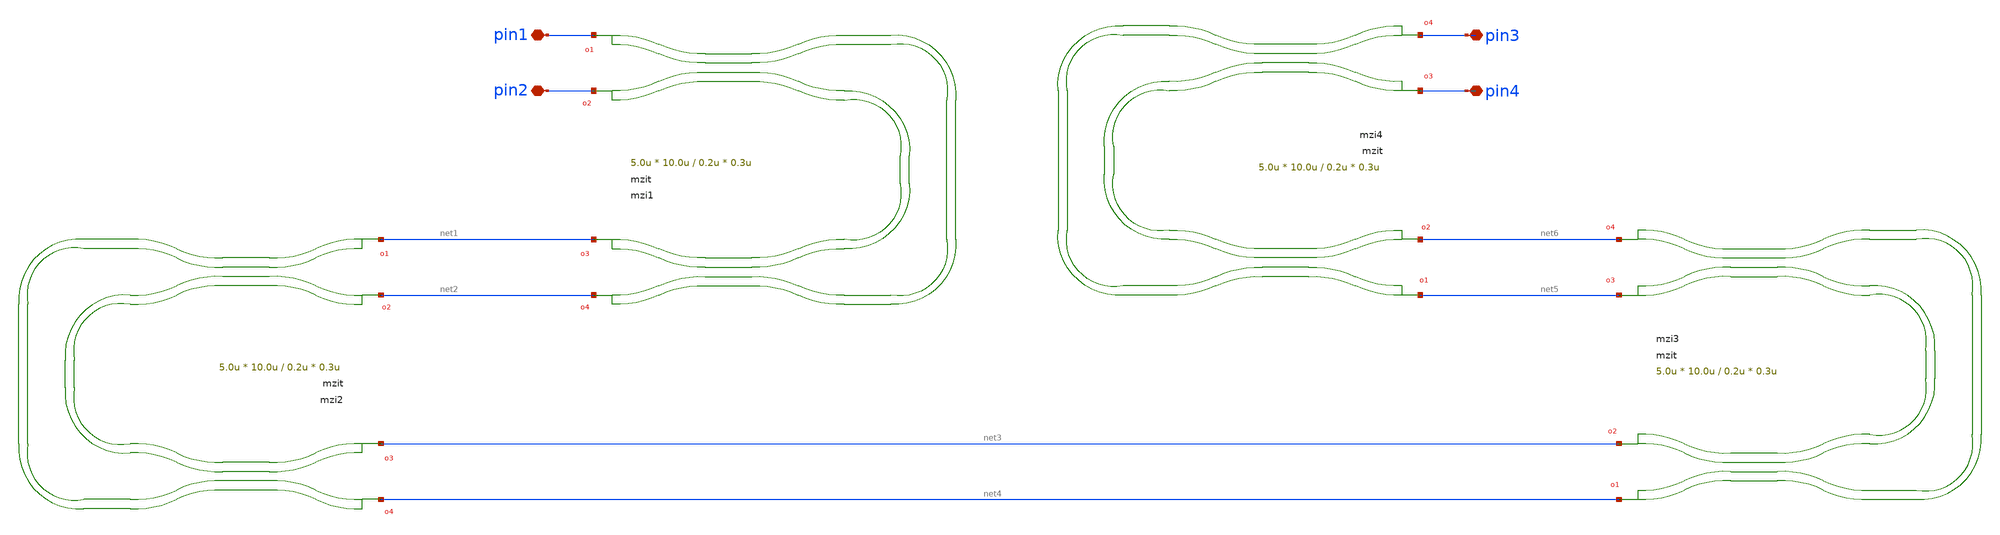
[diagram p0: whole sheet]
** sch_path: xschem/tests/test_sch/test_mzit.sch
* Copyright (c) 2024, Mabrains LLC
* Licensed under the GNU Lesser General Public License, Version 3.0 (the "License");
* you may not use this file except in compliance with the License.
* GNU Lesser General Public License
* Version 3, 29 June 2007
* This program is free software: you can redistribute it and/or modify
* it under the terms of the GNU Lesser General Public License as published
* by the Free Software Foundation, either version 3 of the License, or
* (at your option) any later version.
* This program is distributed in the hope that it will be useful,
* but WITHOUT ANY WARRANTY; without even the implied warranty of
* MERCHANTABILITY or FITNESS FOR A PARTICULAR PURPOSE.  See the
* GNU Lesser General Public License for more details.
* You should have received a copy of the GNU Lesser General Public License
* along with this program.  If not, see <https://www.gnu.org/licenses/>.
* SPDX-License-Identifier: LGPL-3.0
**.subckt test_mzit pin1 pin2 pin3 pin4
*.iopin pin1
*.iopin pin2
*.iopin pin3
*.iopin pin4
Pmzi1 pin1 pin2 net1 net2 mzit w0=0.5u w1=0.45u w2=0.55u dy=2.0u delta_length=10.0u length=1.0u
+ coupler_length1=5.0u coupler_length2=10.0u coupler_gap1=0.2u coupler_gap2=0.3u taper_length=5.0u
Pmzi4 net5 net6 pin4 pin3 mzit w0=0.5u w1=0.45u w2=0.55u dy=2.0u delta_length=10.0u length=1.0u
+ coupler_length1=5.0u coupler_length2=10.0u coupler_gap1=0.2u coupler_gap2=0.3u taper_length=5.0u
Pmzi2 net1 net2 net3 net4 mzit w0=0.5u w1=0.45u w2=0.55u dy=2.0u delta_length=10.0u length=1.0u
+ coupler_length1=5.0u coupler_length2=10.0u coupler_gap1=0.2u coupler_gap2=0.3u taper_length=5.0u
Pmzi3 net4 net3 net5 net6 mzit w0=0.5u w1=0.45u w2=0.55u dy=2.0u delta_length=10.0u length=1.0u
+ coupler_length1=5.0u coupler_length2=10.0u coupler_gap1=0.2u coupler_gap2=0.3u taper_length=5.0u
**.ends
.end
